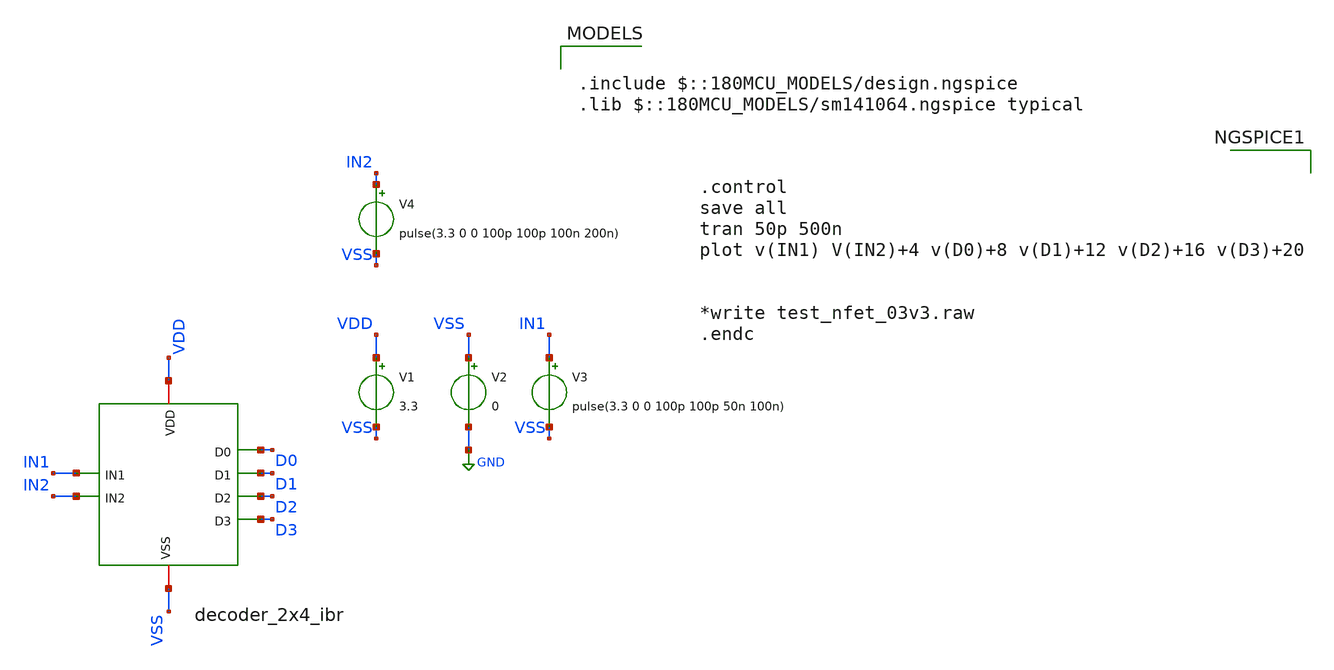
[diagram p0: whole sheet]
** sch_path: Clock_Generator_PAKISTAN_02/Schematics/dec_2x4_test_ibr.sch
**.subckt dec_2x4_test_ibr
V1 VDD VSS 3.3
V2 VSS GND 0
V3 IN1 VSS pulse(3.3 0 0 100p 100p 50n 100n)
V4 IN2 VSS pulse(3.3 0 0 100p 100p 100n 200n)
x1 IN1 VSS VDD D0 D1 D2 D3 IN2 decoder_2x4_ibr
**** begin user architecture code

.include $::180MCU_MODELS/design.ngspice
.lib $::180MCU_MODELS/sm141064.ngspice typical



.control
save all
tran 50p 500n
plot v(IN1) V(IN2)+4 v(D0)+8 v(D1)+12 v(D2)+16 v(D3)+20


*write test_nfet_03v3.raw
.endc


**** end user architecture code
**.ends
.GLOBAL GND
.end
